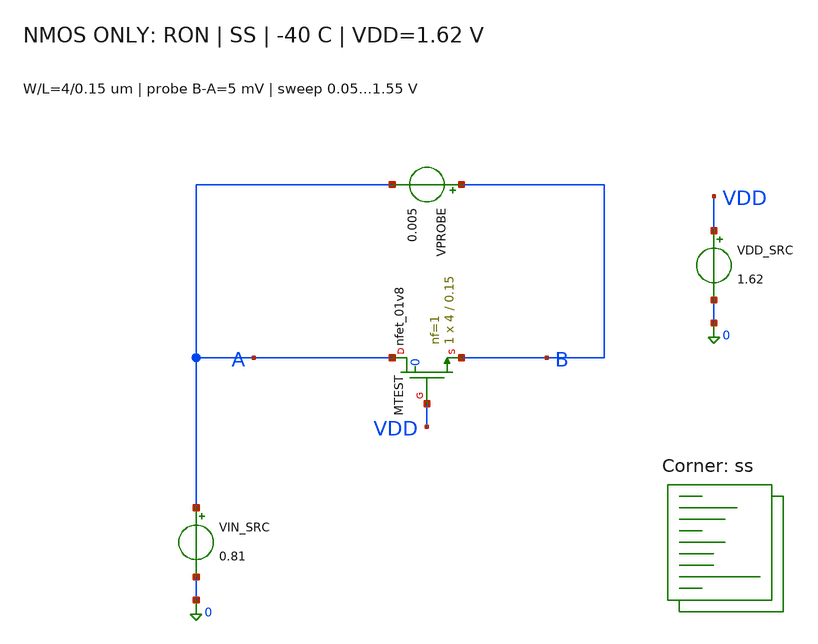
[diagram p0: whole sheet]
** sch_path: blocks/05_Switch_Network/sim/tb_5B_ron_nmos.sch
**.subckt tb_5B_ron_nmos
VPROBE B A 0.005
.save i(vprobe)
VIN_SRC A 0 0.81
VDD_SRC VDD 0 1.62
XMTEST A VDD B 0 sky130_fd_pr__nfet_01v8 L=0.15 W=4 nf=1 ad=1.16 as=1.16 pd=8.58 ps=8.58 nrd=0.0725
+ nrs=0.0725 sa=0 sb=0 sd=0 mult=1 m=1
**** begin user architecture code
.lib $::SKYWATER_MODELS/sky130.lib.spice ss


.option scale=1e-6 reltol=1e-5 abstol=1e-14 vntol=1e-8
.temp -40
.control
save all
set wr_singlescale
set wr_vecnames
set numdgt=15
dc VIN_SRC 0.05 1.55 0.005
let RON=abs((v(B)-v(A))/i(VPROBE))
meas dc RON_MIN MIN RON
meas dc RON_MAX MAX RON
meas dc RON_060 FIND RON AT=0.6
meas dc RON_081 FIND RON AT=0.81
meas dc RON_089 FIND RON AT=0.89
meas dc RON_090 FIND RON AT=0.9
meas dc RON_120 FIND RON AT=1.2
wrdata ron_nmos_ss_1p62_m40.dat v(A) v(B) i(VPROBE) RON
plot RON
.endc


**** end user architecture code
**.ends
.end
